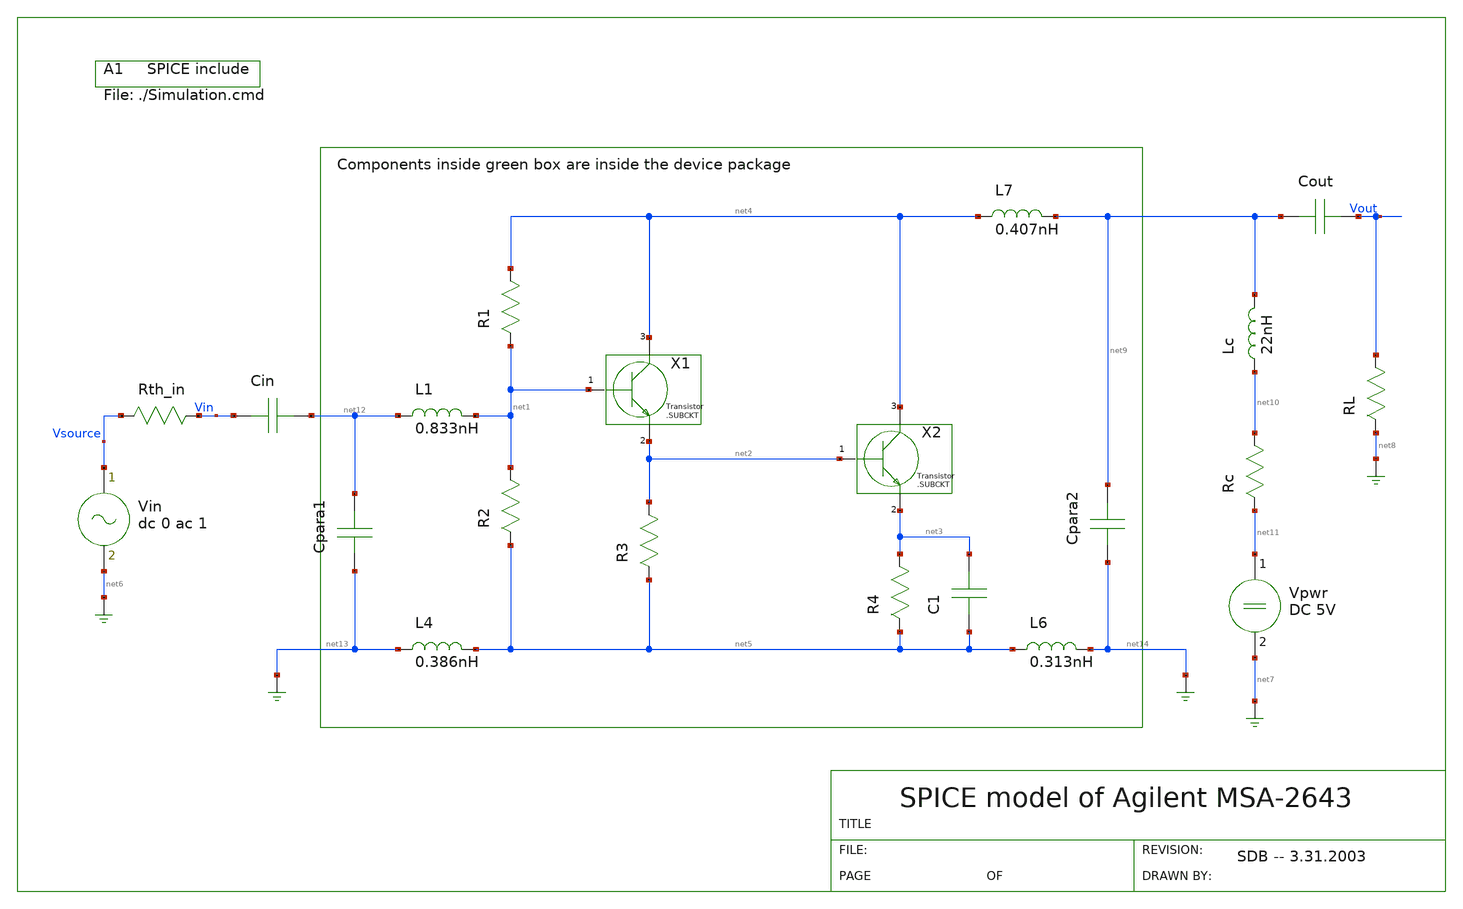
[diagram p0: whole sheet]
** sch_path: xschem_library/gschem_import/MSA-2643.sch
**.subckt MSA-2643
R1 net4 net1 560
R2 net1 net5 660
R3 net2 net5 250
R4 net3 net5 5
X1 net4 net1 net2
X2 net4 net2 net3
C1 net5 net3 4pF
Vpwr net11 net7 DC 5V
Vin Vsource net6 dc 0 ac 1
Rth_in Vin Vsource 50
RL Vout net8 50
Lc net10 net9 22nH
Rc net10 net11 50
Cout net9 Vout 47pF
Cin Vin net12 47pF
.include ./Simulation.cmd
L4 net13 net5 0.386nH
L6 net5 net14 0.313nH
L1 net12 net1 0.833nH
L7 net4 net9 0.407nH
Cpara1 net13 net12 0.158pF
Cpara2 net14 net9 0.155pF
**.ends
.end
